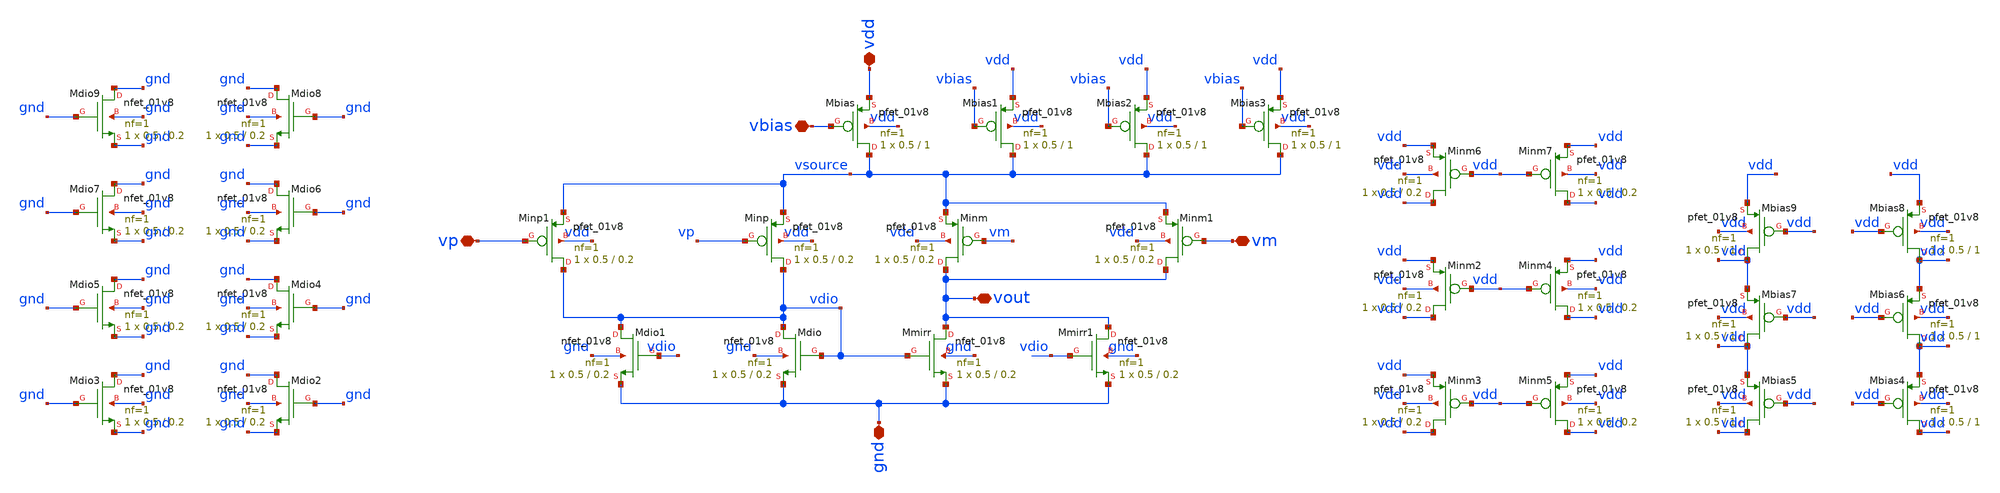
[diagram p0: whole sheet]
** sch_path: analog/xschem/col_amp_n_clamp_v1/amp_p_5T.sch
**.subckt amp_p_5T gnd vdd vout vbias vm vp
*.iopin gnd
*.iopin vdd
*.iopin vout
*.iopin vbias
*.iopin vm
*.iopin vp
XMinm vout vm vsource vdd sky130_fd_pr__pfet_01v8 L=0.2 W=0.5 nf=1 ad='int((1 + 1)/2) * 0.5 / 1 * 0.29'
+ as='int((1 + 2)/2) * 0.5 / 1 * 0.29' pd='2*int((1 + 1)/2) * (0.5 / 1 + 0.29)' ps='2*int((1 + 2)/2) * (0.5 / 1 + 0.29)'
+ nrd='0.29 / 0.5 ' nrs='0.29 / 0.5 ' sa=0 sb=0 sd=0 mult=1 m=1
XMinp vdio vp vsource vdd sky130_fd_pr__pfet_01v8 L=0.2 W=0.5 nf=1 ad='int((1 + 1)/2) * 0.5 / 1 * 0.29'
+ as='int((1 + 2)/2) * 0.5 / 1 * 0.29' pd='2*int((1 + 1)/2) * (0.5 / 1 + 0.29)' ps='2*int((1 + 2)/2) * (0.5 / 1 + 0.29)'
+ nrd='0.29 / 0.5 ' nrs='0.29 / 0.5 ' sa=0 sb=0 sd=0 mult=1 m=1
XMdio vdio vdio gnd gnd sky130_fd_pr__nfet_01v8 L=0.2 W=0.5 nf=1 ad='int((1 + 1)/2) * 0.5 / 1 * 0.29'
+ as='int((1 + 2)/2) * 0.5 / 1 * 0.29' pd='2*int((1 + 1)/2) * (0.5 / 1 + 0.29)' ps='2*int((1 + 2)/2) * (0.5 / 1 + 0.29)'
+ nrd='0.29 / 0.5 ' nrs='0.29 / 0.5 ' sa=0 sb=0 sd=0 mult=1 m=1
XMmirr vout vdio gnd gnd sky130_fd_pr__nfet_01v8 L=0.2 W=0.5 nf=1 ad='int((1 + 1)/2) * 0.5 / 1 * 0.29'
+ as='int((1 + 2)/2) * 0.5 / 1 * 0.29' pd='2*int((1 + 1)/2) * (0.5 / 1 + 0.29)' ps='2*int((1 + 2)/2) * (0.5 / 1 + 0.29)'
+ nrd='0.29 / 0.5 ' nrs='0.29 / 0.5 ' sa=0 sb=0 sd=0 mult=1 m=1
XMbias vsource vbias vdd vdd sky130_fd_pr__pfet_01v8 L=1 W=0.5 nf=1 ad='int((1 + 1)/2) * 0.5 / 1 * 0.29'
+ as='int((1 + 2)/2) * 0.5 / 1 * 0.29' pd='2*int((1 + 1)/2) * (0.5 / 1 + 0.29)' ps='2*int((1 + 2)/2) * (0.5 / 1 + 0.29)'
+ nrd='0.29 / 0.5 ' nrs='0.29 / 0.5 ' sa=0 sb=0 sd=0 mult=1 m=1
XMbias1 vsource vbias vdd vdd sky130_fd_pr__pfet_01v8 L=1 W=0.5 nf=1 ad='int((1 + 1)/2) * 0.5 / 1 * 0.29'
+ as='int((1 + 2)/2) * 0.5 / 1 * 0.29' pd='2*int((1 + 1)/2) * (0.5 / 1 + 0.29)' ps='2*int((1 + 2)/2) * (0.5 / 1 + 0.29)'
+ nrd='0.29 / 0.5 ' nrs='0.29 / 0.5 ' sa=0 sb=0 sd=0 mult=1 m=1
XMbias2 vsource vbias vdd vdd sky130_fd_pr__pfet_01v8 L=1 W=0.5 nf=1 ad='int((1 + 1)/2) * 0.5 / 1 * 0.29'
+ as='int((1 + 2)/2) * 0.5 / 1 * 0.29' pd='2*int((1 + 1)/2) * (0.5 / 1 + 0.29)' ps='2*int((1 + 2)/2) * (0.5 / 1 + 0.29)'
+ nrd='0.29 / 0.5 ' nrs='0.29 / 0.5 ' sa=0 sb=0 sd=0 mult=1 m=1
XMbias3 vsource vbias vdd vdd sky130_fd_pr__pfet_01v8 L=1 W=0.5 nf=1 ad='int((1 + 1)/2) * 0.5 / 1 * 0.29'
+ as='int((1 + 2)/2) * 0.5 / 1 * 0.29' pd='2*int((1 + 1)/2) * (0.5 / 1 + 0.29)' ps='2*int((1 + 2)/2) * (0.5 / 1 + 0.29)'
+ nrd='0.29 / 0.5 ' nrs='0.29 / 0.5 ' sa=0 sb=0 sd=0 mult=1 m=1
XMmirr1 vout vdio gnd gnd sky130_fd_pr__nfet_01v8 L=0.2 W=0.5 nf=1 ad='int((1 + 1)/2) * 0.5 / 1 * 0.29'
+ as='int((1 + 2)/2) * 0.5 / 1 * 0.29' pd='2*int((1 + 1)/2) * (0.5 / 1 + 0.29)' ps='2*int((1 + 2)/2) * (0.5 / 1 + 0.29)'
+ nrd='0.29 / 0.5 ' nrs='0.29 / 0.5 ' sa=0 sb=0 sd=0 mult=1 m=1
XMdio1 vdio vdio gnd gnd sky130_fd_pr__nfet_01v8 L=0.2 W=0.5 nf=1 ad='int((1 + 1)/2) * 0.5 / 1 * 0.29'
+ as='int((1 + 2)/2) * 0.5 / 1 * 0.29' pd='2*int((1 + 1)/2) * (0.5 / 1 + 0.29)' ps='2*int((1 + 2)/2) * (0.5 / 1 + 0.29)'
+ nrd='0.29 / 0.5 ' nrs='0.29 / 0.5 ' sa=0 sb=0 sd=0 mult=1 m=1
XMinm1 vout vm vsource vdd sky130_fd_pr__pfet_01v8 L=0.2 W=0.5 nf=1 ad='int((1 + 1)/2) * 0.5 / 1 * 0.29'
+ as='int((1 + 2)/2) * 0.5 / 1 * 0.29' pd='2*int((1 + 1)/2) * (0.5 / 1 + 0.29)' ps='2*int((1 + 2)/2) * (0.5 / 1 + 0.29)'
+ nrd='0.29 / 0.5 ' nrs='0.29 / 0.5 ' sa=0 sb=0 sd=0 mult=1 m=1
XMinp1 vdio vp vsource vdd sky130_fd_pr__pfet_01v8 L=0.2 W=0.5 nf=1 ad='int((1 + 1)/2) * 0.5 / 1 * 0.29'
+ as='int((1 + 2)/2) * 0.5 / 1 * 0.29' pd='2*int((1 + 1)/2) * (0.5 / 1 + 0.29)' ps='2*int((1 + 2)/2) * (0.5 / 1 + 0.29)'
+ nrd='0.29 / 0.5 ' nrs='0.29 / 0.5 ' sa=0 sb=0 sd=0 mult=1 m=1
XMinm2 vdd vdd vdd vdd sky130_fd_pr__pfet_01v8 L=0.2 W=0.5 nf=1 ad='int((1 + 1)/2) * 0.5 / 1 * 0.29'
+ as='int((1 + 2)/2) * 0.5 / 1 * 0.29' pd='2*int((1 + 1)/2) * (0.5 / 1 + 0.29)' ps='2*int((1 + 2)/2) * (0.5 / 1 + 0.29)'
+ nrd='0.29 / 0.5 ' nrs='0.29 / 0.5 ' sa=0 sb=0 sd=0 mult=1 m=1
XMinm3 vdd vdd vdd vdd sky130_fd_pr__pfet_01v8 L=0.2 W=0.5 nf=1 ad='int((1 + 1)/2) * 0.5 / 1 * 0.29'
+ as='int((1 + 2)/2) * 0.5 / 1 * 0.29' pd='2*int((1 + 1)/2) * (0.5 / 1 + 0.29)' ps='2*int((1 + 2)/2) * (0.5 / 1 + 0.29)'
+ nrd='0.29 / 0.5 ' nrs='0.29 / 0.5 ' sa=0 sb=0 sd=0 mult=1 m=1
XMinm4 vdd vdd vdd vdd sky130_fd_pr__pfet_01v8 L=0.2 W=0.5 nf=1 ad='int((1 + 1)/2) * 0.5 / 1 * 0.29'
+ as='int((1 + 2)/2) * 0.5 / 1 * 0.29' pd='2*int((1 + 1)/2) * (0.5 / 1 + 0.29)' ps='2*int((1 + 2)/2) * (0.5 / 1 + 0.29)'
+ nrd='0.29 / 0.5 ' nrs='0.29 / 0.5 ' sa=0 sb=0 sd=0 mult=1 m=1
XMinm5 vdd vdd vdd vdd sky130_fd_pr__pfet_01v8 L=0.2 W=0.5 nf=1 ad='int((1 + 1)/2) * 0.5 / 1 * 0.29'
+ as='int((1 + 2)/2) * 0.5 / 1 * 0.29' pd='2*int((1 + 1)/2) * (0.5 / 1 + 0.29)' ps='2*int((1 + 2)/2) * (0.5 / 1 + 0.29)'
+ nrd='0.29 / 0.5 ' nrs='0.29 / 0.5 ' sa=0 sb=0 sd=0 mult=1 m=1
XMdio2 gnd gnd gnd gnd sky130_fd_pr__nfet_01v8 L=0.2 W=0.5 nf=1 ad='int((1 + 1)/2) * 0.5 / 1 * 0.29'
+ as='int((1 + 2)/2) * 0.5 / 1 * 0.29' pd='2*int((1 + 1)/2) * (0.5 / 1 + 0.29)' ps='2*int((1 + 2)/2) * (0.5 / 1 + 0.29)'
+ nrd='0.29 / 0.5 ' nrs='0.29 / 0.5 ' sa=0 sb=0 sd=0 mult=1 m=1
XMdio3 gnd gnd gnd gnd sky130_fd_pr__nfet_01v8 L=0.2 W=0.5 nf=1 ad='int((1 + 1)/2) * 0.5 / 1 * 0.29'
+ as='int((1 + 2)/2) * 0.5 / 1 * 0.29' pd='2*int((1 + 1)/2) * (0.5 / 1 + 0.29)' ps='2*int((1 + 2)/2) * (0.5 / 1 + 0.29)'
+ nrd='0.29 / 0.5 ' nrs='0.29 / 0.5 ' sa=0 sb=0 sd=0 mult=1 m=1
XMdio4 gnd gnd gnd gnd sky130_fd_pr__nfet_01v8 L=0.2 W=0.5 nf=1 ad='int((1 + 1)/2) * 0.5 / 1 * 0.29'
+ as='int((1 + 2)/2) * 0.5 / 1 * 0.29' pd='2*int((1 + 1)/2) * (0.5 / 1 + 0.29)' ps='2*int((1 + 2)/2) * (0.5 / 1 + 0.29)'
+ nrd='0.29 / 0.5 ' nrs='0.29 / 0.5 ' sa=0 sb=0 sd=0 mult=1 m=1
XMdio5 gnd gnd gnd gnd sky130_fd_pr__nfet_01v8 L=0.2 W=0.5 nf=1 ad='int((1 + 1)/2) * 0.5 / 1 * 0.29'
+ as='int((1 + 2)/2) * 0.5 / 1 * 0.29' pd='2*int((1 + 1)/2) * (0.5 / 1 + 0.29)' ps='2*int((1 + 2)/2) * (0.5 / 1 + 0.29)'
+ nrd='0.29 / 0.5 ' nrs='0.29 / 0.5 ' sa=0 sb=0 sd=0 mult=1 m=1
XMdio6 gnd gnd gnd gnd sky130_fd_pr__nfet_01v8 L=0.2 W=0.5 nf=1 ad='int((1 + 1)/2) * 0.5 / 1 * 0.29'
+ as='int((1 + 2)/2) * 0.5 / 1 * 0.29' pd='2*int((1 + 1)/2) * (0.5 / 1 + 0.29)' ps='2*int((1 + 2)/2) * (0.5 / 1 + 0.29)'
+ nrd='0.29 / 0.5 ' nrs='0.29 / 0.5 ' sa=0 sb=0 sd=0 mult=1 m=1
XMdio7 gnd gnd gnd gnd sky130_fd_pr__nfet_01v8 L=0.2 W=0.5 nf=1 ad='int((1 + 1)/2) * 0.5 / 1 * 0.29'
+ as='int((1 + 2)/2) * 0.5 / 1 * 0.29' pd='2*int((1 + 1)/2) * (0.5 / 1 + 0.29)' ps='2*int((1 + 2)/2) * (0.5 / 1 + 0.29)'
+ nrd='0.29 / 0.5 ' nrs='0.29 / 0.5 ' sa=0 sb=0 sd=0 mult=1 m=1
XMdio8 gnd gnd gnd gnd sky130_fd_pr__nfet_01v8 L=0.2 W=0.5 nf=1 ad='int((1 + 1)/2) * 0.5 / 1 * 0.29'
+ as='int((1 + 2)/2) * 0.5 / 1 * 0.29' pd='2*int((1 + 1)/2) * (0.5 / 1 + 0.29)' ps='2*int((1 + 2)/2) * (0.5 / 1 + 0.29)'
+ nrd='0.29 / 0.5 ' nrs='0.29 / 0.5 ' sa=0 sb=0 sd=0 mult=1 m=1
XMdio9 gnd gnd gnd gnd sky130_fd_pr__nfet_01v8 L=0.2 W=0.5 nf=1 ad='int((1 + 1)/2) * 0.5 / 1 * 0.29'
+ as='int((1 + 2)/2) * 0.5 / 1 * 0.29' pd='2*int((1 + 1)/2) * (0.5 / 1 + 0.29)' ps='2*int((1 + 2)/2) * (0.5 / 1 + 0.29)'
+ nrd='0.29 / 0.5 ' nrs='0.29 / 0.5 ' sa=0 sb=0 sd=0 mult=1 m=1
XMinm6 vdd vdd vdd vdd sky130_fd_pr__pfet_01v8 L=0.2 W=0.5 nf=1 ad='int((1 + 1)/2) * 0.5 / 1 * 0.29'
+ as='int((1 + 2)/2) * 0.5 / 1 * 0.29' pd='2*int((1 + 1)/2) * (0.5 / 1 + 0.29)' ps='2*int((1 + 2)/2) * (0.5 / 1 + 0.29)'
+ nrd='0.29 / 0.5 ' nrs='0.29 / 0.5 ' sa=0 sb=0 sd=0 mult=1 m=1
XMinm7 vdd vdd vdd vdd sky130_fd_pr__pfet_01v8 L=0.2 W=0.5 nf=1 ad='int((1 + 1)/2) * 0.5 / 1 * 0.29'
+ as='int((1 + 2)/2) * 0.5 / 1 * 0.29' pd='2*int((1 + 1)/2) * (0.5 / 1 + 0.29)' ps='2*int((1 + 2)/2) * (0.5 / 1 + 0.29)'
+ nrd='0.29 / 0.5 ' nrs='0.29 / 0.5 ' sa=0 sb=0 sd=0 mult=1 m=1
XMbias4 vdd vdd vdd vdd sky130_fd_pr__pfet_01v8 L=1 W=0.5 nf=1 ad='int((1 + 1)/2) * 0.5 / 1 * 0.29' as='int((1 + 2)/2) * 0.5 / 1 * 0.29'
+ pd='2*int((1 + 1)/2) * (0.5 / 1 + 0.29)' ps='2*int((1 + 2)/2) * (0.5 / 1 + 0.29)' nrd='0.29 / 0.5 ' nrs='0.29 / 0.5 '
+ sa=0 sb=0 sd=0 mult=1 m=1
XMbias5 vdd vdd vdd vdd sky130_fd_pr__pfet_01v8 L=1 W=0.5 nf=1 ad='int((1 + 1)/2) * 0.5 / 1 * 0.29' as='int((1 + 2)/2) * 0.5 / 1 * 0.29'
+ pd='2*int((1 + 1)/2) * (0.5 / 1 + 0.29)' ps='2*int((1 + 2)/2) * (0.5 / 1 + 0.29)' nrd='0.29 / 0.5 ' nrs='0.29 / 0.5 '
+ sa=0 sb=0 sd=0 mult=1 m=1
XMbias6 vdd vdd vdd vdd sky130_fd_pr__pfet_01v8 L=1 W=0.5 nf=1 ad='int((1 + 1)/2) * 0.5 / 1 * 0.29' as='int((1 + 2)/2) * 0.5 / 1 * 0.29'
+ pd='2*int((1 + 1)/2) * (0.5 / 1 + 0.29)' ps='2*int((1 + 2)/2) * (0.5 / 1 + 0.29)' nrd='0.29 / 0.5 ' nrs='0.29 / 0.5 '
+ sa=0 sb=0 sd=0 mult=1 m=1
XMbias7 vdd vdd vdd vdd sky130_fd_pr__pfet_01v8 L=1 W=0.5 nf=1 ad='int((1 + 1)/2) * 0.5 / 1 * 0.29' as='int((1 + 2)/2) * 0.5 / 1 * 0.29'
+ pd='2*int((1 + 1)/2) * (0.5 / 1 + 0.29)' ps='2*int((1 + 2)/2) * (0.5 / 1 + 0.29)' nrd='0.29 / 0.5 ' nrs='0.29 / 0.5 '
+ sa=0 sb=0 sd=0 mult=1 m=1
XMbias8 vdd vdd vdd vdd sky130_fd_pr__pfet_01v8 L=1 W=0.5 nf=1 ad='int((1 + 1)/2) * 0.5 / 1 * 0.29' as='int((1 + 2)/2) * 0.5 / 1 * 0.29'
+ pd='2*int((1 + 1)/2) * (0.5 / 1 + 0.29)' ps='2*int((1 + 2)/2) * (0.5 / 1 + 0.29)' nrd='0.29 / 0.5 ' nrs='0.29 / 0.5 '
+ sa=0 sb=0 sd=0 mult=1 m=1
XMbias9 vdd vdd vdd vdd sky130_fd_pr__pfet_01v8 L=1 W=0.5 nf=1 ad='int((1 + 1)/2) * 0.5 / 1 * 0.29' as='int((1 + 2)/2) * 0.5 / 1 * 0.29'
+ pd='2*int((1 + 1)/2) * (0.5 / 1 + 0.29)' ps='2*int((1 + 2)/2) * (0.5 / 1 + 0.29)' nrd='0.29 / 0.5 ' nrs='0.29 / 0.5 '
+ sa=0 sb=0 sd=0 mult=1 m=1
**.ends
.end
